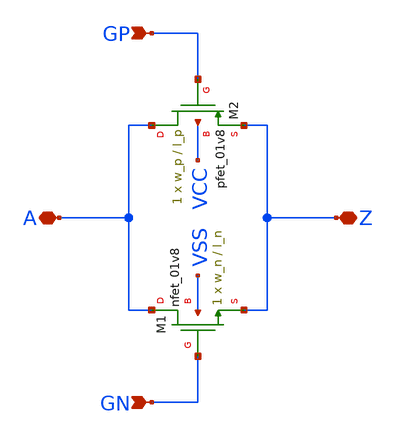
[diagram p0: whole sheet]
** sch_path: sky130_tests_ng/passgate.sch
* Copyright 2020 Stefan Frederik Schippers
* Licensed under the Apache License, Version 2.0 (the "License");
* you may not use this file except in compliance with the License.
* You may obtain a copy of the License at
* https://www.apache.org/licenses/LICENSE-2.0
* Unless required by applicable law or agreed to in writing, software
* distributed under the License is distributed on an "AS IS" BASIS,
* WITHOUT WARRANTIES OR CONDITIONS OF ANY KIND, either express or implied.
* See the License for the specific language governing permissions and
* limitations under the License.
**.subckt passgate A Z GP GN
*.iopin A
*.iopin Z
*.ipin GP
*.ipin GN
XM1 A GN Z VSS sky130_fd_pr__nfet_01v8 W=w_n L=l_n ad='w * 0.29u' pd='w + 2 * 0.29u' as='w * 0.29u' ps='w + 2 * 0.29u'
+ nrd=0 nrs=0 sa=0 sb=0 sd=0 nf=1 mult=1
XM2 A GP Z VCC sky130_fd_pr__pfet_01v8 W=w_p L=l_p ad='w * 0.29u' pd='w + 2 * 0.29u' as='w * 0.29u' ps='w + 2 * 0.29u'
+ nrd=0 nrs=0 sa=0 sb=0 sd=0 nf=1 mult=1
**.ends
.end
